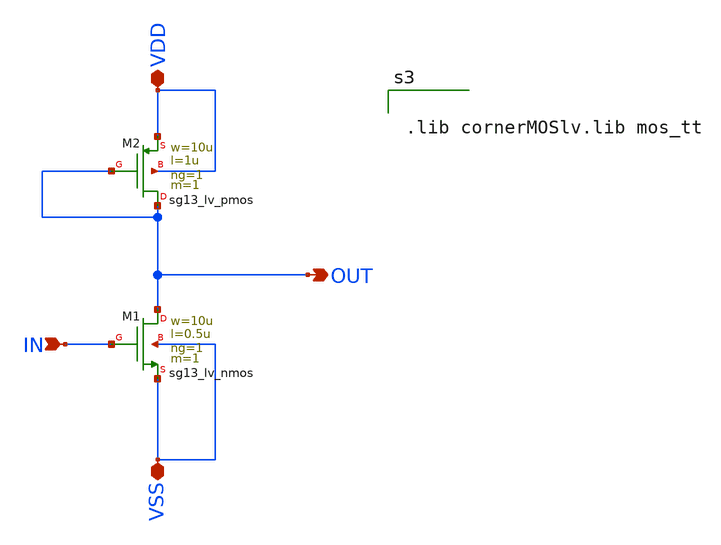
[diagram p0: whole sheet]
** sch_path: BTDay3-Ex/CS_Amplifier_Diode.sch
**.subckt CS_Amplifier_Diode IN VSS OUT VDD
*.ipin IN
*.iopin VSS
*.opin OUT
*.iopin VDD
XM1 OUT IN VSS VSS sg13_lv_nmos w=10u l=0.5u ng=1 m=1 mm_ok=1
XM2 OUT OUT VDD VDD sg13_lv_pmos w=10u l=1u ng=1 m=1 mm_ok=1
**** begin user architecture code


.lib cornerMOSlv.lib mos_tt


**** end user architecture code
**.ends
.end
